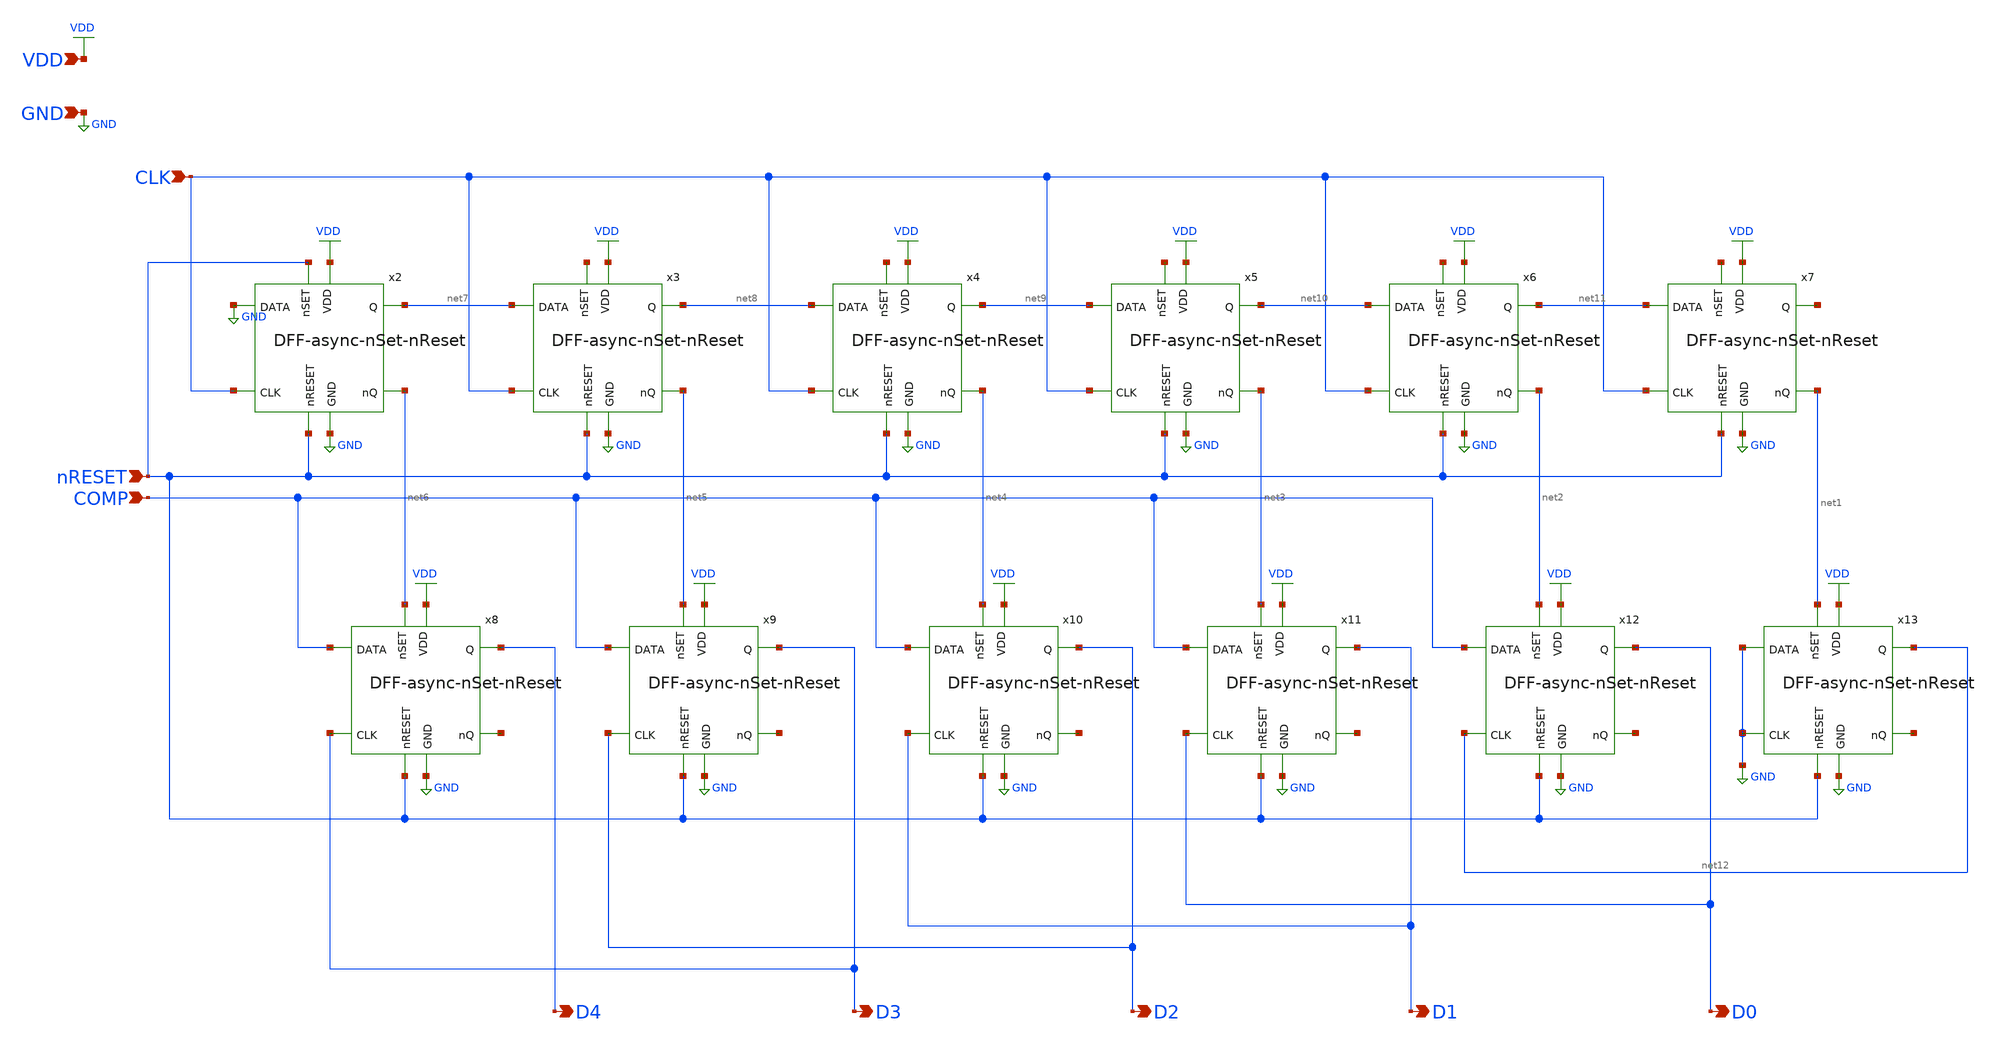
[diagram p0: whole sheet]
** sch_path: analog/schematics/SAR-Logic.sch
**.subckt SAR-Logic CLK nRESET COMP GND VDD D0 D1 D2 D3 D4
*.ipin CLK
*.ipin nRESET
*.ipin COMP
*.ipin GND
*.ipin VDD
*.opin D0
*.opin D1
*.opin D2
*.opin D3
*.opin D4
x2 nRESET net7 VDD CLK net6 GND nRESET GND DFF-async-nSet-nReset
x3 net13 net8 VDD CLK net5 GND nRESET net7 DFF-async-nSet-nReset
x4 net14 net9 VDD CLK net4 GND nRESET net8 DFF-async-nSet-nReset
x5 net15 net10 VDD CLK net3 GND nRESET net9 DFF-async-nSet-nReset
x6 net16 net11 VDD CLK net2 GND nRESET net10 DFF-async-nSet-nReset
x7 net17 net18 VDD CLK net1 GND nRESET net11 DFF-async-nSet-nReset
x8 net6 D4 VDD D3 net19 GND nRESET COMP DFF-async-nSet-nReset
x9 net5 D3 VDD D2 net20 GND nRESET COMP DFF-async-nSet-nReset
x10 net4 D2 VDD D1 net21 GND nRESET COMP DFF-async-nSet-nReset
x11 net3 D1 VDD D0 net22 GND nRESET COMP DFF-async-nSet-nReset
x12 net2 D0 VDD net12 net23 GND nRESET COMP DFF-async-nSet-nReset
x13 net1 net12 VDD GND net24 GND nRESET GND DFF-async-nSet-nReset
**.ends
.GLOBAL GND
.GLOBAL VDD
.end
